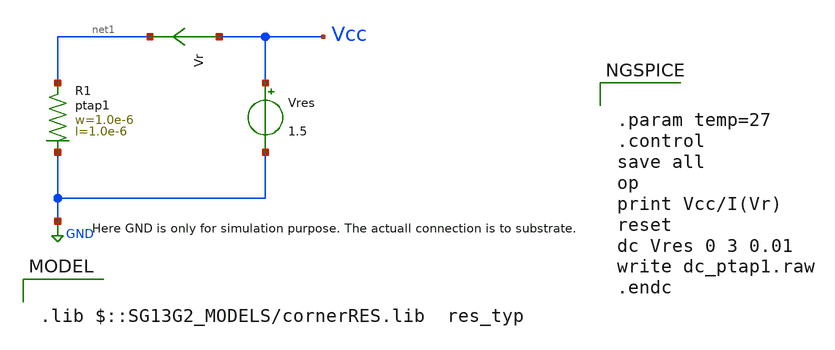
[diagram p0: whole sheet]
** sch_path: ihp-sg13g2/libs.tech/xschem/sg13g2_tests/dc_ptap1.sch
* Copyright 2023 IHP PDK Authors
**.subckt dc_ptap1
Vres Vcc GND 1.5
Vr Vcc net1 0
.save i(vr)
XR1 net1 GND ptap1 R=196 w=1.0e-6 l=1.0e-6
**** begin user architecture code

.lib $::SG13G2_MODELS/cornerRES.lib  res_typ



.param temp=27
.control
save all
op
print Vcc/I(Vr)
reset
dc Vres 0 3 0.01
write dc_ptap1.raw
.endc


**** end user architecture code
**.ends
.GLOBAL GND
.end
